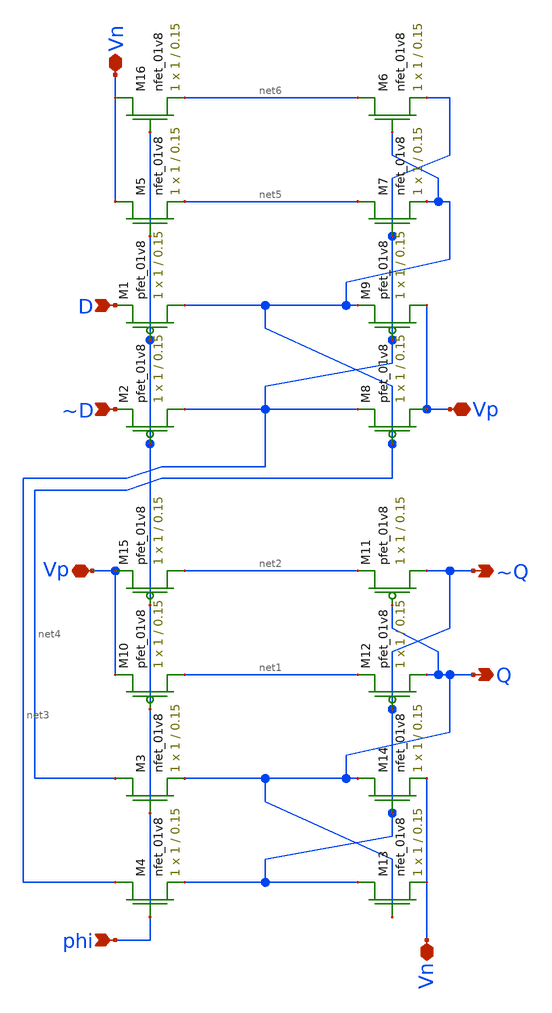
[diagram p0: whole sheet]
** sch_path: mini_proj_2/schematic/dff_3.sch
**.subckt dff_3 phi D ~D Vp ~Q Q Vn Vp Vn
*.ipin phi
*.ipin D
*.ipin ~D
*.iopin Vp
*.opin ~Q
*.opin Q
*.iopin Vn
*.iopin Vp
*.iopin Vn
XM4 net3 phi ~Q GND sky130_fd_pr__nfet_01v8 L=0.15 W=1 nf=1 ad='int((nf+1)/2) * W/nf * 0.29' as='int((nf+2)/2) * W/nf * 0.29'
+ pd='2*int((nf+1)/2) * (W/nf + 0.29)' ps='2*int((nf+2)/2) * (W/nf + 0.29)' nrd='0.29 / W' nrs='0.29 / W'
+ sa=0 sb=0 sd=0 mult=1 m=1
XM3 net4 phi Q GND sky130_fd_pr__nfet_01v8 L=0.15 W=1 nf=1 ad='int((nf+1)/2) * W/nf * 0.29' as='int((nf+2)/2) * W/nf * 0.29'
+ pd='2*int((nf+1)/2) * (W/nf + 0.29)' ps='2*int((nf+2)/2) * (W/nf + 0.29)' nrd='0.29 / W' nrs='0.29 / W'
+ sa=0 sb=0 sd=0 mult=1 m=1
XM1 net4 phi D VDD sky130_fd_pr__pfet_01v8 L=0.15 W=1 nf=1 ad='int((nf+1)/2) * W/nf * 0.29' as='int((nf+2)/2) * W/nf * 0.29'
+ pd='2*int((nf+1)/2) * (W/nf + 0.29)' ps='2*int((nf+2)/2) * (W/nf + 0.29)' nrd='0.29 / W' nrs='0.29 / W'
+ sa=0 sb=0 sd=0 mult=1 m=1
XM2 net3 phi ~D VDD sky130_fd_pr__pfet_01v8 L=0.15 W=1 nf=1 ad='int((nf+1)/2) * W/nf * 0.29' as='int((nf+2)/2) * W/nf * 0.29'
+ pd='2*int((nf+1)/2) * (W/nf + 0.29)' ps='2*int((nf+2)/2) * (W/nf + 0.29)' nrd='0.29 / W' nrs='0.29 / W'
+ sa=0 sb=0 sd=0 mult=1 m=1
XM10 net1 phi Vp VDD sky130_fd_pr__pfet_01v8 L=0.15 W=1 nf=1 ad='int((nf+1)/2) * W/nf * 0.29' as='int((nf+2)/2) * W/nf * 0.29'
+ pd='2*int((nf+1)/2) * (W/nf + 0.29)' ps='2*int((nf+2)/2) * (W/nf + 0.29)' nrd='0.29 / W' nrs='0.29 / W'
+ sa=0 sb=0 sd=0 mult=1 m=1
XM13 ~Q Q Vn GND sky130_fd_pr__nfet_01v8 L=0.15 W=1 nf=1 ad='int((nf+1)/2) * W/nf * 0.29' as='int((nf+2)/2) * W/nf * 0.29'
+ pd='2*int((nf+1)/2) * (W/nf + 0.29)' ps='2*int((nf+2)/2) * (W/nf + 0.29)' nrd='0.29 / W' nrs='0.29 / W'
+ sa=0 sb=0 sd=0 mult=1 m=1
XM14 Q ~Q Vn GND sky130_fd_pr__nfet_01v8 L=0.15 W=1 nf=1 ad='int((nf+1)/2) * W/nf * 0.29' as='int((nf+2)/2) * W/nf * 0.29'
+ pd='2*int((nf+1)/2) * (W/nf + 0.29)' ps='2*int((nf+2)/2) * (W/nf + 0.29)' nrd='0.29 / W' nrs='0.29 / W'
+ sa=0 sb=0 sd=0 mult=1 m=1
XM6 net6 net4 net3 GND sky130_fd_pr__nfet_01v8 L=0.15 W=1 nf=1 ad='int((nf+1)/2) * W/nf * 0.29' as='int((nf+2)/2) * W/nf * 0.29'
+ pd='2*int((nf+1)/2) * (W/nf + 0.29)' ps='2*int((nf+2)/2) * (W/nf + 0.29)' nrd='0.29 / W' nrs='0.29 / W'
+ sa=0 sb=0 sd=0 mult=1 m=1
XM7 net5 net3 net4 GND sky130_fd_pr__nfet_01v8 L=0.15 W=1 nf=1 ad='int((nf+1)/2) * W/nf * 0.29' as='int((nf+2)/2) * W/nf * 0.29'
+ pd='2*int((nf+1)/2) * (W/nf + 0.29)' ps='2*int((nf+2)/2) * (W/nf + 0.29)' nrd='0.29 / W' nrs='0.29 / W'
+ sa=0 sb=0 sd=0 mult=1 m=1
XM5 Vn phi net5 GND sky130_fd_pr__nfet_01v8 L=0.15 W=1 nf=1 ad='int((nf+1)/2) * W/nf * 0.29' as='int((nf+2)/2) * W/nf * 0.29'
+ pd='2*int((nf+1)/2) * (W/nf + 0.29)' ps='2*int((nf+2)/2) * (W/nf + 0.29)' nrd='0.29 / W' nrs='0.29 / W'
+ sa=0 sb=0 sd=0 mult=1 m=1
XM8 Vp net4 net3 VDD sky130_fd_pr__pfet_01v8 L=0.15 W=1 nf=1 ad='int((nf+1)/2) * W/nf * 0.29' as='int((nf+2)/2) * W/nf * 0.29'
+ pd='2*int((nf+1)/2) * (W/nf + 0.29)' ps='2*int((nf+2)/2) * (W/nf + 0.29)' nrd='0.29 / W' nrs='0.29 / W'
+ sa=0 sb=0 sd=0 mult=1 m=1
XM9 Vp net3 net4 VDD sky130_fd_pr__pfet_01v8 L=0.15 W=1 nf=1 ad='int((nf+1)/2) * W/nf * 0.29' as='int((nf+2)/2) * W/nf * 0.29'
+ pd='2*int((nf+1)/2) * (W/nf + 0.29)' ps='2*int((nf+2)/2) * (W/nf + 0.29)' nrd='0.29 / W' nrs='0.29 / W'
+ sa=0 sb=0 sd=0 mult=1 m=1
XM12 Q ~Q net1 VDD sky130_fd_pr__pfet_01v8 L=0.15 W=1 nf=1 ad='int((nf+1)/2) * W/nf * 0.29' as='int((nf+2)/2) * W/nf * 0.29'
+ pd='2*int((nf+1)/2) * (W/nf + 0.29)' ps='2*int((nf+2)/2) * (W/nf + 0.29)' nrd='0.29 / W' nrs='0.29 / W'
+ sa=0 sb=0 sd=0 mult=1 m=1
XM11 ~Q Q net2 VDD sky130_fd_pr__pfet_01v8 L=0.15 W=1 nf=1 ad='int((nf+1)/2) * W/nf * 0.29' as='int((nf+2)/2) * W/nf * 0.29'
+ pd='2*int((nf+1)/2) * (W/nf + 0.29)' ps='2*int((nf+2)/2) * (W/nf + 0.29)' nrd='0.29 / W' nrs='0.29 / W'
+ sa=0 sb=0 sd=0 mult=1 m=1
XM16 Vn phi net6 GND sky130_fd_pr__nfet_01v8 L=0.15 W=1 nf=1 ad='int((nf+1)/2) * W/nf * 0.29' as='int((nf+2)/2) * W/nf * 0.29'
+ pd='2*int((nf+1)/2) * (W/nf + 0.29)' ps='2*int((nf+2)/2) * (W/nf + 0.29)' nrd='0.29 / W' nrs='0.29 / W'
+ sa=0 sb=0 sd=0 mult=1 m=1
XM15 net2 phi Vp VDD sky130_fd_pr__pfet_01v8 L=0.15 W=1 nf=1 ad='int((nf+1)/2) * W/nf * 0.29' as='int((nf+2)/2) * W/nf * 0.29'
+ pd='2*int((nf+1)/2) * (W/nf + 0.29)' ps='2*int((nf+2)/2) * (W/nf + 0.29)' nrd='0.29 / W' nrs='0.29 / W'
+ sa=0 sb=0 sd=0 mult=1 m=1
**.ends
.end
